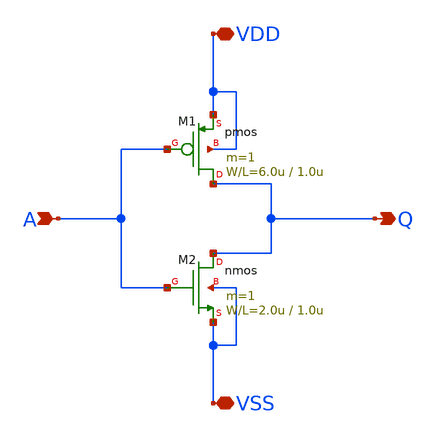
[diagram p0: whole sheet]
** sch_path: member_project/arstopia/tk-inverter.sch
**.subckt tk-inverter VDD VSS A Q
*.iopin VDD
*.iopin VSS
*.ipin A
*.opin Q
M1 Q A VDD VDD pmos L=1.0u W=6.0u m=1
M2 Q A VSS VSS nmos L=1.0u W=2.0u m=1
**.ends
.end
